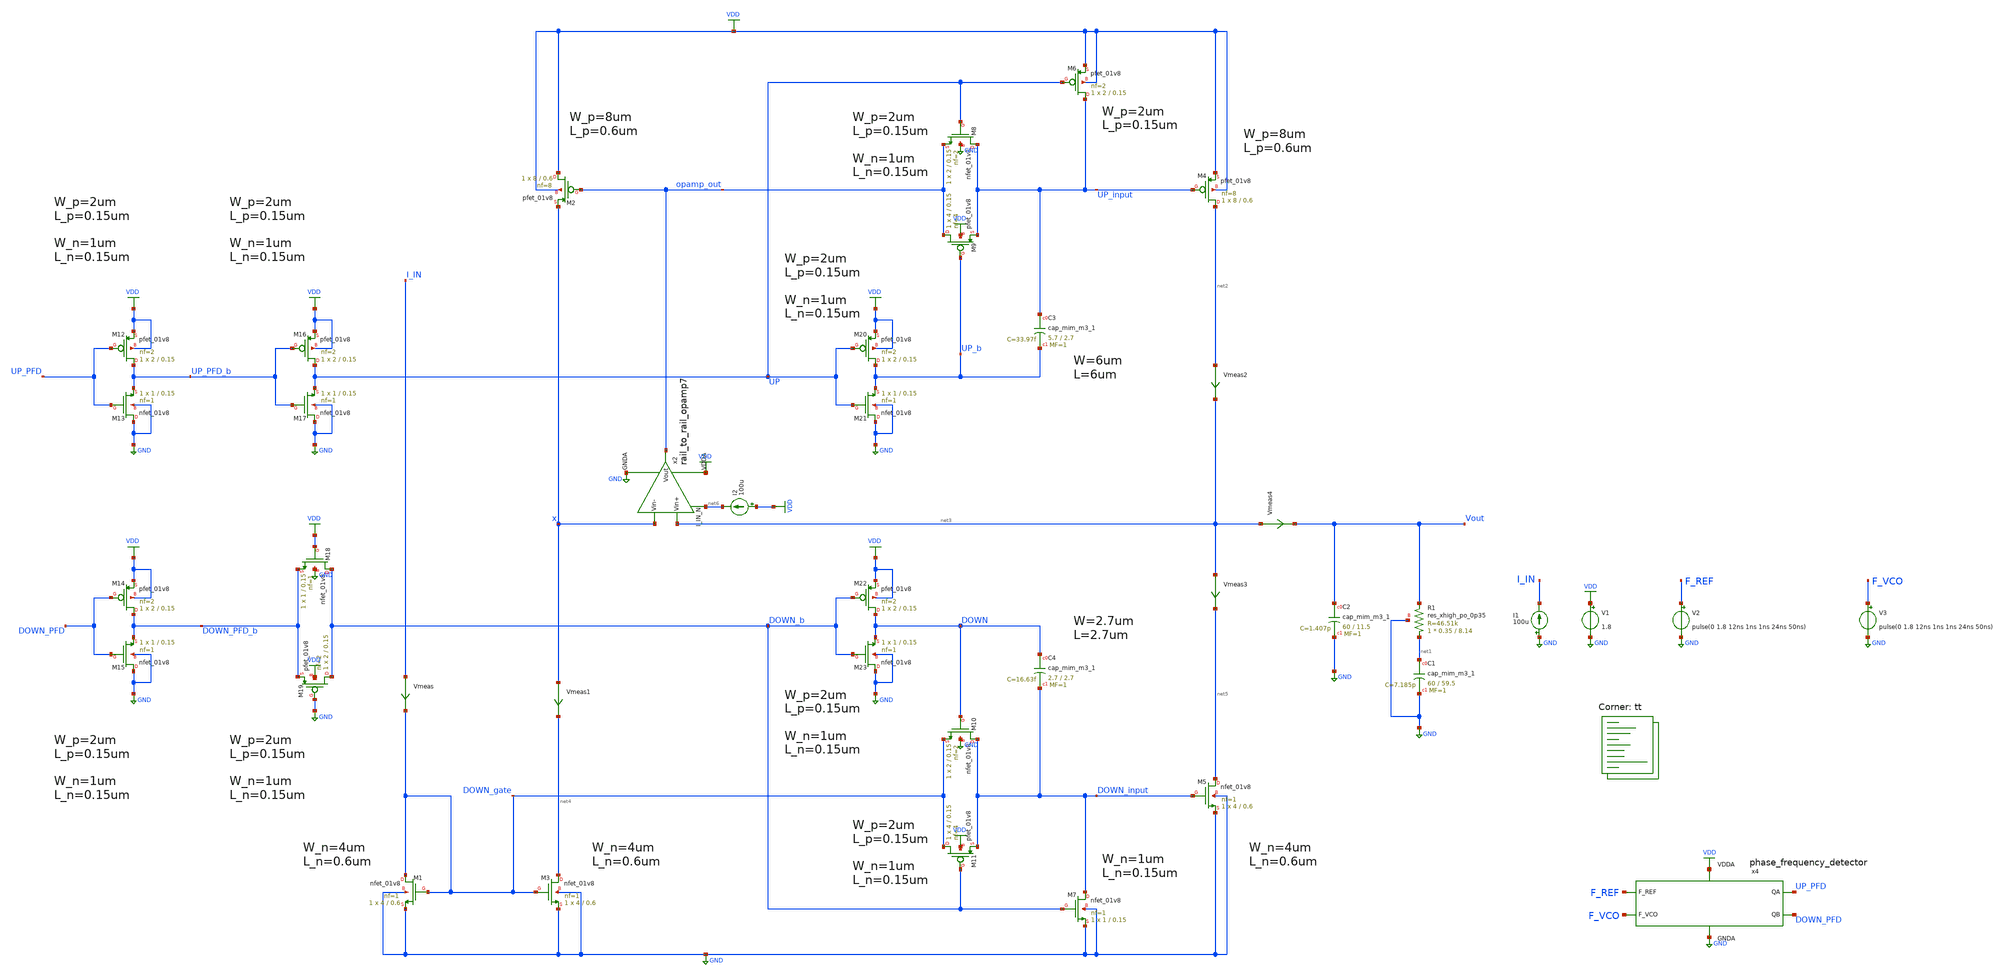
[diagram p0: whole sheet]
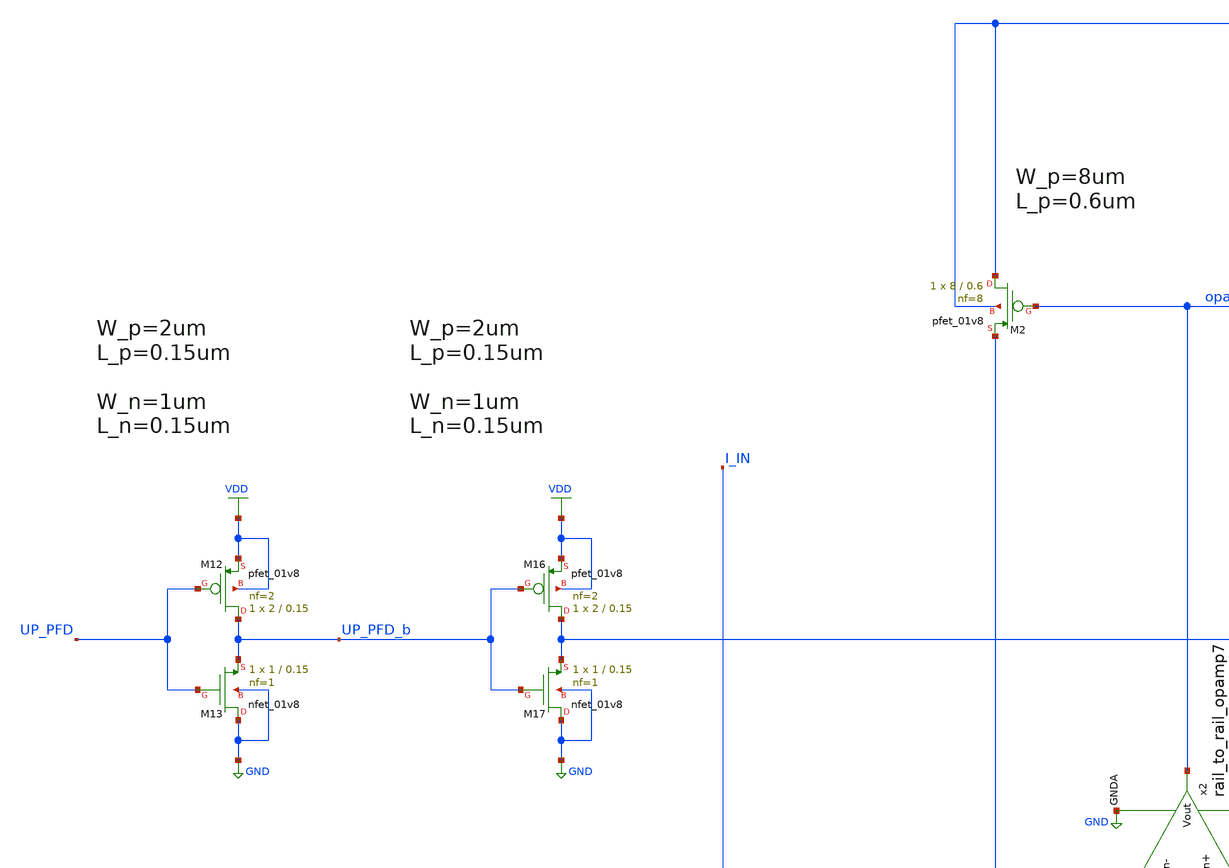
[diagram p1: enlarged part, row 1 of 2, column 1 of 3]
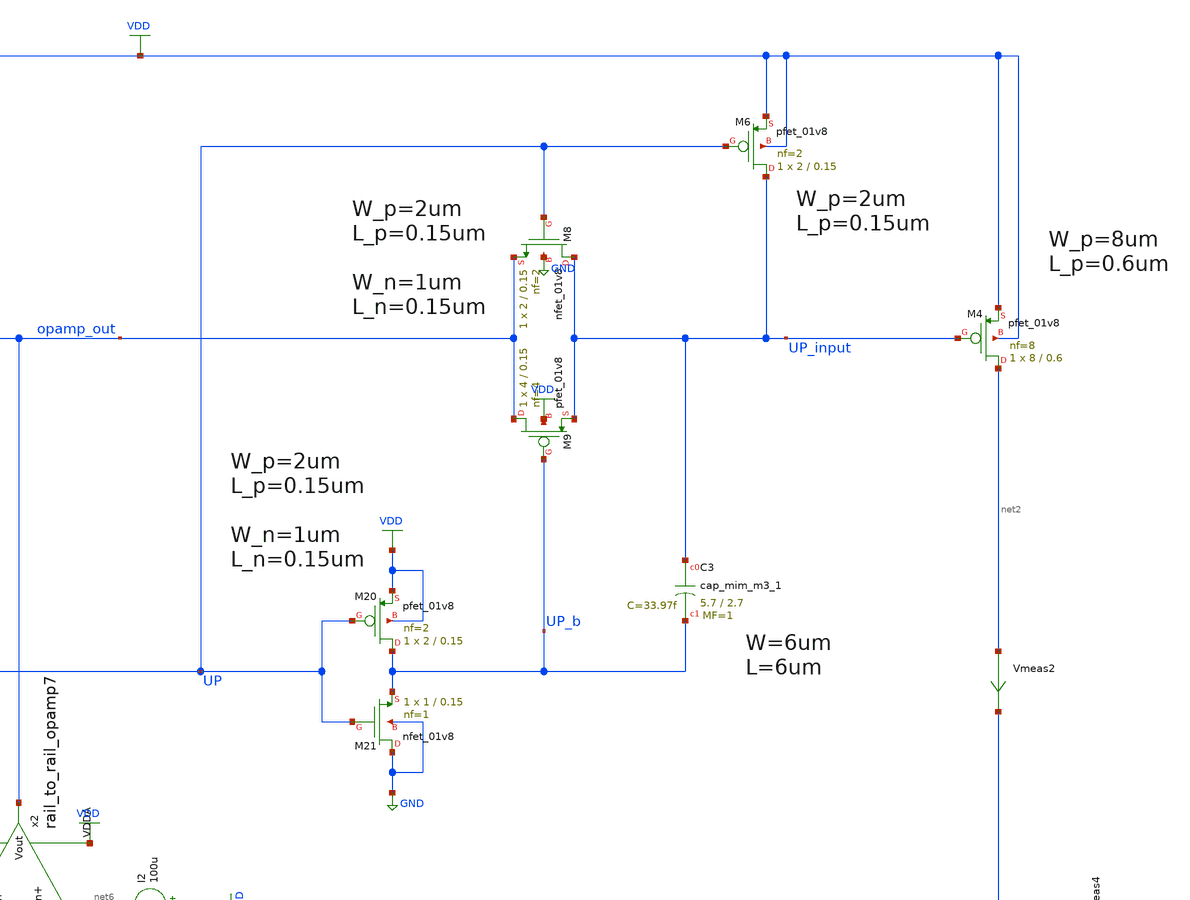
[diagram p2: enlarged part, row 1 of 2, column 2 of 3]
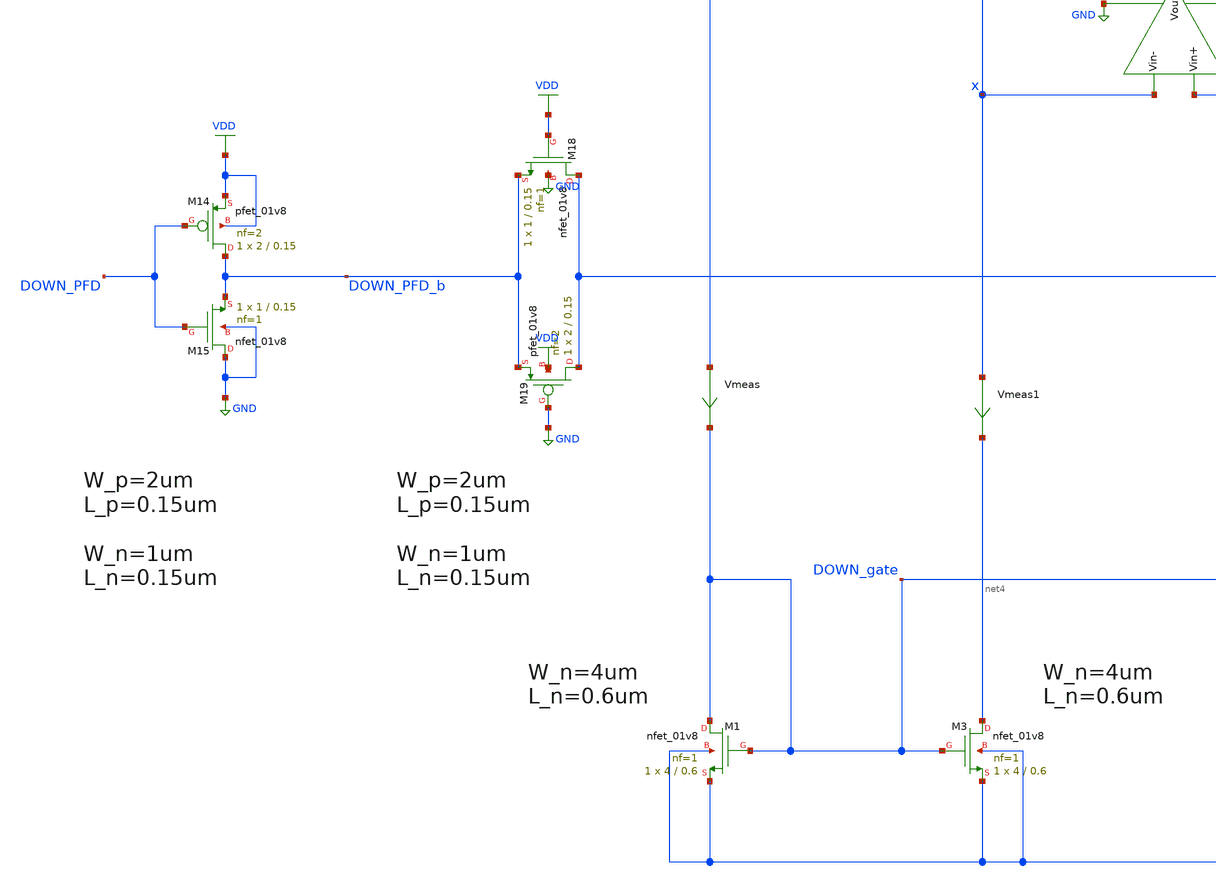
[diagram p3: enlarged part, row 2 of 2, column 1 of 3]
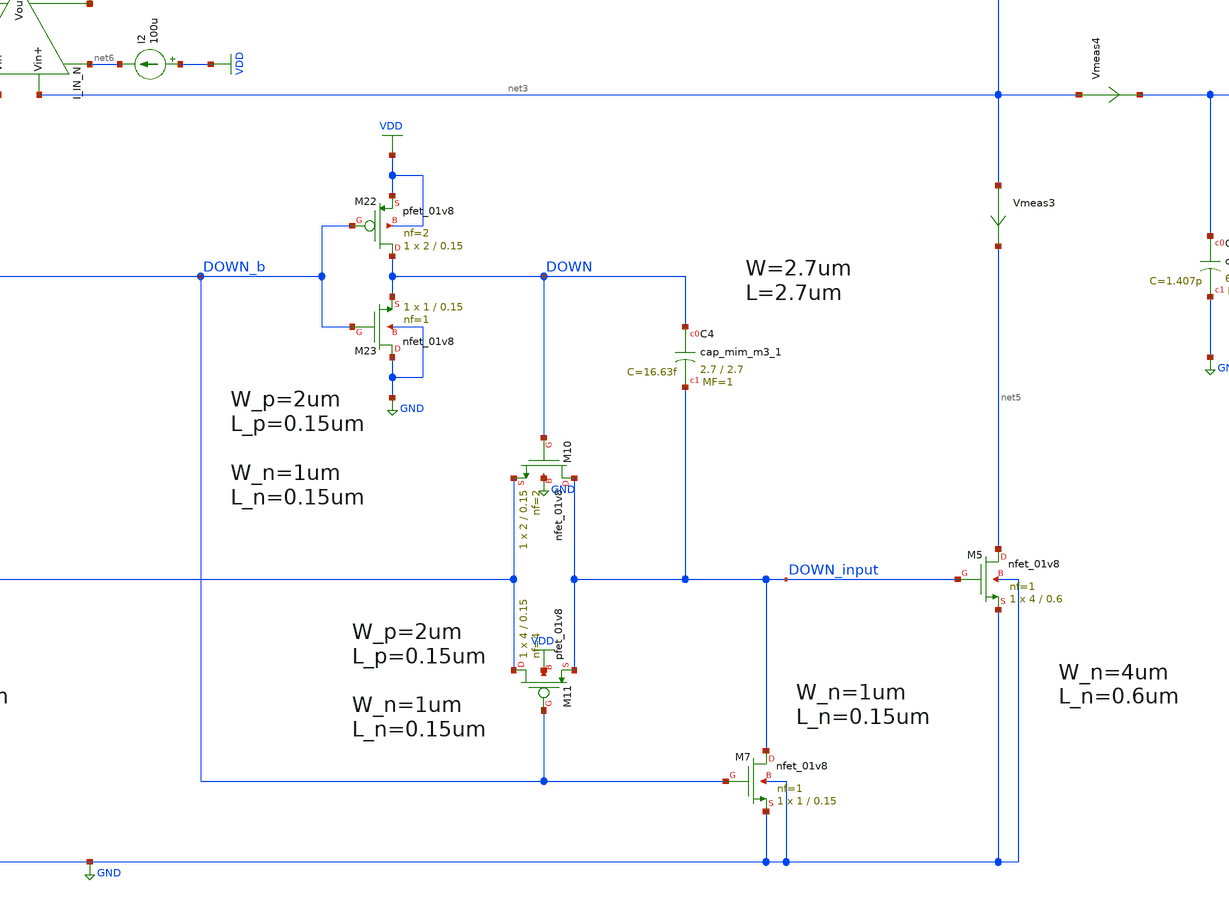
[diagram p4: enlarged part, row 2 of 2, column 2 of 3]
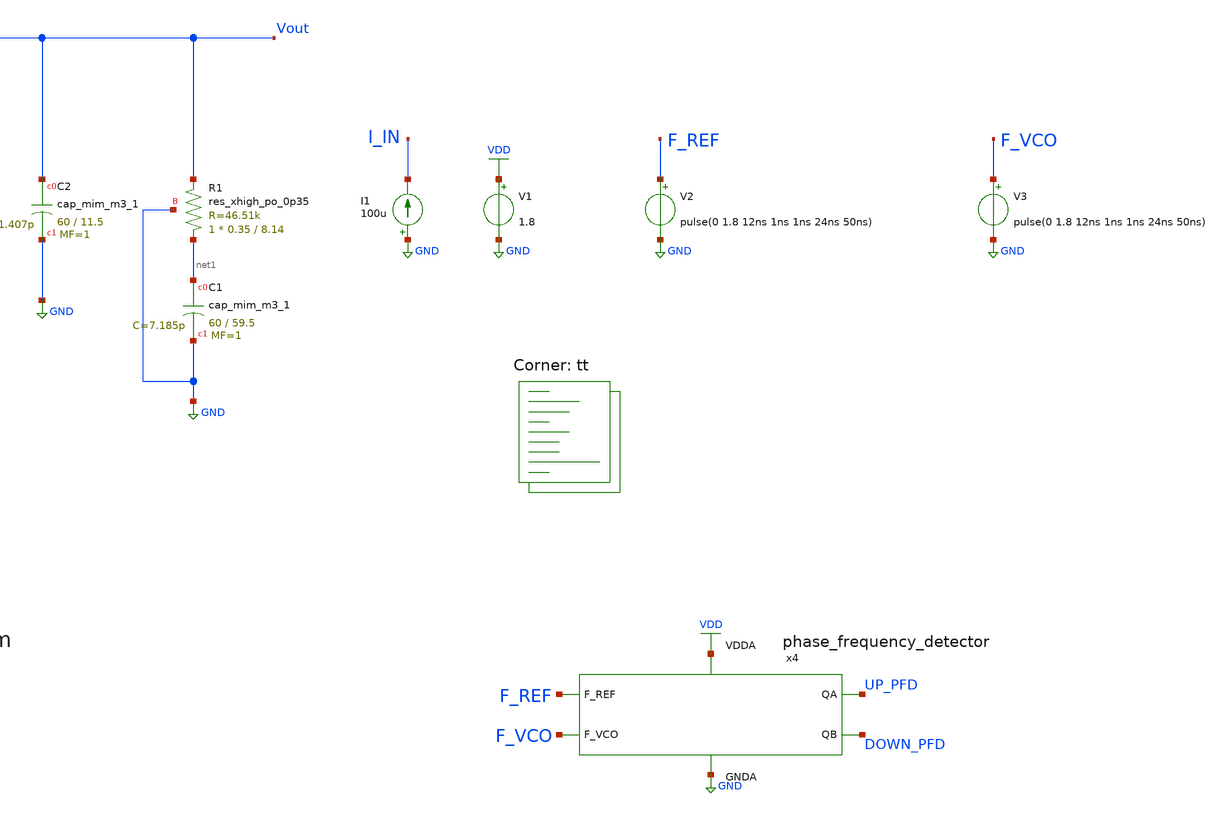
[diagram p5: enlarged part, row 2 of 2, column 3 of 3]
** sch_path: projects/pll/charge_pump/xschem_ngspice/pfd_charge_pump_13.sch
**.subckt pfd_charge_pump_13
V1 VDD GND 1.8
XC2 Vout GND sky130_fd_pr__cap_mim_m3_1 W=60 L=11.5 MF=1 m=1
XC1 net1 GND sky130_fd_pr__cap_mim_m3_1 W=60 L=59.5 MF=1 m=1
V2 F_REF GND pulse(0 1.8 12ns 1ns 1ns 24ns 50ns)
V3 F_VCO GND pulse(0 1.8 12ns 1ns 1ns 24ns 50ns)
x4 F_REF F_VCO VDD UP_PFD DOWN_PFD GND phase_frequency_detector
XR1 net1 Vout GND sky130_fd_pr__res_xhigh_po_0p35 L=8.14 mult=1 m=1
I1 GND I_IN 100u
Vmeas3 net3 net5 0
.save i(vmeas3)
XM1 DOWN_gate DOWN_gate GND GND sky130_fd_pr__nfet_01v8 L=0.6 W=4 nf=1 ad='int((nf+1)/2) * W/nf * 0.29'
+ as='int((nf+2)/2) * W/nf * 0.29' pd='2*int((nf+1)/2) * (W/nf + 0.29)' ps='2*int((nf+2)/2) * (W/nf + 0.29)'
+ nrd='0.29 / W' nrs='0.29 / W' sa=0 sb=0 sd=0 mult=1 m=1
XM3 net4 DOWN_gate GND GND sky130_fd_pr__nfet_01v8 L=0.6 W=4 nf=1 ad='int((nf+1)/2) * W/nf * 0.29' as='int((nf+2)/2) * W/nf * 0.29'
+ pd='2*int((nf+1)/2) * (W/nf + 0.29)' ps='2*int((nf+2)/2) * (W/nf + 0.29)' nrd='0.29 / W' nrs='0.29 / W'
+ sa=0 sb=0 sd=0 mult=1 m=1
XM2 VDD opamp_out x VDD sky130_fd_pr__pfet_01v8 L=0.6 W=8 nf=8 ad='int((nf+1)/2) * W/nf * 0.29' as='int((nf+2)/2) * W/nf * 0.29'
+ pd='2*int((nf+1)/2) * (W/nf + 0.29)' ps='2*int((nf+2)/2) * (W/nf + 0.29)' nrd='0.29 / W' nrs='0.29 / W'
+ sa=0 sb=0 sd=0 mult=1 m=1
XM9 opamp_out UP_b UP_input VDD sky130_fd_pr__pfet_01v8 L=0.15 W=4 nf=4 ad='int((nf+1)/2) * W/nf * 0.29'
+ as='int((nf+2)/2) * W/nf * 0.29' pd='2*int((nf+1)/2) * (W/nf + 0.29)' ps='2*int((nf+2)/2) * (W/nf + 0.29)'
+ nrd='0.29 / W' nrs='0.29 / W' sa=0 sb=0 sd=0 mult=1 m=1
XM6 UP_input UP VDD VDD sky130_fd_pr__pfet_01v8 L=0.15 W=2 nf=2 ad='int((nf+1)/2) * W/nf * 0.29' as='int((nf+2)/2) * W/nf * 0.29'
+ pd='2*int((nf+1)/2) * (W/nf + 0.29)' ps='2*int((nf+2)/2) * (W/nf + 0.29)' nrd='0.29 / W' nrs='0.29 / W'
+ sa=0 sb=0 sd=0 mult=1 m=1
XM4 net2 UP_input VDD VDD sky130_fd_pr__pfet_01v8 L=0.6 W=8 nf=8 ad='int((nf+1)/2) * W/nf * 0.29' as='int((nf+2)/2) * W/nf * 0.29'
+ pd='2*int((nf+1)/2) * (W/nf + 0.29)' ps='2*int((nf+2)/2) * (W/nf + 0.29)' nrd='0.29 / W' nrs='0.29 / W'
+ sa=0 sb=0 sd=0 mult=1 m=1
XM10 DOWN_input DOWN DOWN_gate GND sky130_fd_pr__nfet_01v8 L=0.15 W=2 nf=2 ad='int((nf+1)/2) * W/nf * 0.29'
+ as='int((nf+2)/2) * W/nf * 0.29' pd='2*int((nf+1)/2) * (W/nf + 0.29)' ps='2*int((nf+2)/2) * (W/nf + 0.29)'
+ nrd='0.29 / W' nrs='0.29 / W' sa=0 sb=0 sd=0 mult=1 m=1
XM7 DOWN_input DOWN_b GND GND sky130_fd_pr__nfet_01v8 L=0.15 W=1 nf=1 ad='int((nf+1)/2) * W/nf * 0.29'
+ as='int((nf+2)/2) * W/nf * 0.29' pd='2*int((nf+1)/2) * (W/nf + 0.29)' ps='2*int((nf+2)/2) * (W/nf + 0.29)'
+ nrd='0.29 / W' nrs='0.29 / W' sa=0 sb=0 sd=0 mult=1 m=1
XM5 net5 DOWN_input GND GND sky130_fd_pr__nfet_01v8 L=0.6 W=4 nf=1 ad='int((nf+1)/2) * W/nf * 0.29' as='int((nf+2)/2) * W/nf * 0.29'
+ pd='2*int((nf+1)/2) * (W/nf + 0.29)' ps='2*int((nf+2)/2) * (W/nf + 0.29)' nrd='0.29 / W' nrs='0.29 / W'
+ sa=0 sb=0 sd=0 mult=1 m=1
x2 net6 VDD net3 x opamp_out GND rail_to_rail_opamp7
XM19 DOWN_b GND DOWN_PFD_b VDD sky130_fd_pr__pfet_01v8 L=0.15 W=2 nf=2 ad='int((nf+1)/2) * W/nf * 0.29'
+ as='int((nf+2)/2) * W/nf * 0.29' pd='2*int((nf+1)/2) * (W/nf + 0.29)' ps='2*int((nf+2)/2) * (W/nf + 0.29)'
+ nrd='0.29 / W' nrs='0.29 / W' sa=0 sb=0 sd=0 mult=1 m=1
XM18 DOWN_b VDD DOWN_PFD_b GND sky130_fd_pr__nfet_01v8 L=0.15 W=1 nf=1 ad='int((nf+1)/2) * W/nf * 0.29'
+ as='int((nf+2)/2) * W/nf * 0.29' pd='2*int((nf+1)/2) * (W/nf + 0.29)' ps='2*int((nf+2)/2) * (W/nf + 0.29)'
+ nrd='0.29 / W' nrs='0.29 / W' sa=0 sb=0 sd=0 mult=1 m=1
XM14 DOWN_PFD_b DOWN_PFD VDD VDD sky130_fd_pr__pfet_01v8 L=0.15 W=2 nf=2 ad='int((nf+1)/2) * W/nf * 0.29'
+ as='int((nf+2)/2) * W/nf * 0.29' pd='2*int((nf+1)/2) * (W/nf + 0.29)' ps='2*int((nf+2)/2) * (W/nf + 0.29)'
+ nrd='0.29 / W' nrs='0.29 / W' sa=0 sb=0 sd=0 mult=1 m=1
XM15 GND DOWN_PFD DOWN_PFD_b GND sky130_fd_pr__nfet_01v8 L=0.15 W=1 nf=1 ad='int((nf+1)/2) * W/nf * 0.29'
+ as='int((nf+2)/2) * W/nf * 0.29' pd='2*int((nf+1)/2) * (W/nf + 0.29)' ps='2*int((nf+2)/2) * (W/nf + 0.29)'
+ nrd='0.29 / W' nrs='0.29 / W' sa=0 sb=0 sd=0 mult=1 m=1
XM12 UP_PFD_b UP_PFD VDD VDD sky130_fd_pr__pfet_01v8 L=0.15 W=2 nf=2 ad='int((nf+1)/2) * W/nf * 0.29'
+ as='int((nf+2)/2) * W/nf * 0.29' pd='2*int((nf+1)/2) * (W/nf + 0.29)' ps='2*int((nf+2)/2) * (W/nf + 0.29)'
+ nrd='0.29 / W' nrs='0.29 / W' sa=0 sb=0 sd=0 mult=1 m=1
XM13 GND UP_PFD UP_PFD_b GND sky130_fd_pr__nfet_01v8 L=0.15 W=1 nf=1 ad='int((nf+1)/2) * W/nf * 0.29'
+ as='int((nf+2)/2) * W/nf * 0.29' pd='2*int((nf+1)/2) * (W/nf + 0.29)' ps='2*int((nf+2)/2) * (W/nf + 0.29)'
+ nrd='0.29 / W' nrs='0.29 / W' sa=0 sb=0 sd=0 mult=1 m=1
XM16 UP UP_PFD_b VDD VDD sky130_fd_pr__pfet_01v8 L=0.15 W=2 nf=2 ad='int((nf+1)/2) * W/nf * 0.29' as='int((nf+2)/2) * W/nf * 0.29'
+ pd='2*int((nf+1)/2) * (W/nf + 0.29)' ps='2*int((nf+2)/2) * (W/nf + 0.29)' nrd='0.29 / W' nrs='0.29 / W'
+ sa=0 sb=0 sd=0 mult=1 m=1
XM17 GND UP_PFD_b UP GND sky130_fd_pr__nfet_01v8 L=0.15 W=1 nf=1 ad='int((nf+1)/2) * W/nf * 0.29' as='int((nf+2)/2) * W/nf * 0.29'
+ pd='2*int((nf+1)/2) * (W/nf + 0.29)' ps='2*int((nf+2)/2) * (W/nf + 0.29)' nrd='0.29 / W' nrs='0.29 / W'
+ sa=0 sb=0 sd=0 mult=1 m=1
XM22 DOWN DOWN_b VDD VDD sky130_fd_pr__pfet_01v8 L=0.15 W=2 nf=2 ad='int((nf+1)/2) * W/nf * 0.29' as='int((nf+2)/2) * W/nf * 0.29'
+ pd='2*int((nf+1)/2) * (W/nf + 0.29)' ps='2*int((nf+2)/2) * (W/nf + 0.29)' nrd='0.29 / W' nrs='0.29 / W'
+ sa=0 sb=0 sd=0 mult=1 m=1
XM23 GND DOWN_b DOWN GND sky130_fd_pr__nfet_01v8 L=0.15 W=1 nf=1 ad='int((nf+1)/2) * W/nf * 0.29' as='int((nf+2)/2) * W/nf * 0.29'
+ pd='2*int((nf+1)/2) * (W/nf + 0.29)' ps='2*int((nf+2)/2) * (W/nf + 0.29)' nrd='0.29 / W' nrs='0.29 / W'
+ sa=0 sb=0 sd=0 mult=1 m=1
XM20 UP_b UP VDD VDD sky130_fd_pr__pfet_01v8 L=0.15 W=2 nf=2 ad='int((nf+1)/2) * W/nf * 0.29' as='int((nf+2)/2) * W/nf * 0.29'
+ pd='2*int((nf+1)/2) * (W/nf + 0.29)' ps='2*int((nf+2)/2) * (W/nf + 0.29)' nrd='0.29 / W' nrs='0.29 / W'
+ sa=0 sb=0 sd=0 mult=1 m=1
XM21 GND UP UP_b GND sky130_fd_pr__nfet_01v8 L=0.15 W=1 nf=1 ad='int((nf+1)/2) * W/nf * 0.29' as='int((nf+2)/2) * W/nf * 0.29'
+ pd='2*int((nf+1)/2) * (W/nf + 0.29)' ps='2*int((nf+2)/2) * (W/nf + 0.29)' nrd='0.29 / W' nrs='0.29 / W'
+ sa=0 sb=0 sd=0 mult=1 m=1
Vmeas I_IN DOWN_gate 0
.save i(vmeas)
Vmeas1 x net4 0
.save i(vmeas1)
Vmeas2 net2 net3 0
.save i(vmeas2)
Vmeas4 net3 Vout 0
.save i(vmeas4)
XM8 UP_input UP opamp_out GND sky130_fd_pr__nfet_01v8 L=0.15 W=2 nf=2 ad='int((nf+1)/2) * W/nf * 0.29'
+ as='int((nf+2)/2) * W/nf * 0.29' pd='2*int((nf+1)/2) * (W/nf + 0.29)' ps='2*int((nf+2)/2) * (W/nf + 0.29)'
+ nrd='0.29 / W' nrs='0.29 / W' sa=0 sb=0 sd=0 mult=1 m=1
XM11 DOWN_gate DOWN_b DOWN_input VDD sky130_fd_pr__pfet_01v8 L=0.15 W=4 nf=4 ad='int((nf+1)/2) * W/nf * 0.29'
+ as='int((nf+2)/2) * W/nf * 0.29' pd='2*int((nf+1)/2) * (W/nf + 0.29)' ps='2*int((nf+2)/2) * (W/nf + 0.29)'
+ nrd='0.29 / W' nrs='0.29 / W' sa=0 sb=0 sd=0 mult=1 m=1
XC3 UP_input UP_b sky130_fd_pr__cap_mim_m3_1 W=5.7 L=2.7 MF=1 m=1
XC4 DOWN DOWN_input sky130_fd_pr__cap_mim_m3_1 W=2.7 L=2.7 MF=1 m=1
I2 VDD net6 100u
**** begin user architecture code
.lib $::SKYWATER_MODELS/sky130.lib.spice tt



.include /foss/pdks/sky130A/libs.ref/sky130_fd_sc_hd/spice/sky130_fd_sc_hd.spice

.option method=gear
.option wnflag=1
.option savecurrents

.save @m.x2.xm11.msky130_fd_pr__pfet_01v8[gm] @m.x2.xm12.msky130_fd_pr__nfet_01v8[gm]

* V_out initial voltage value for the F_VCO delay of 2ns  (leading)
* .ic v(vout) = 1.8

* V_out initial voltage value for the F_VCO delay of 12ns (lock condition)
.ic v(vout) = 0.83

* V_out initial voltage value for the F_VCO delay of 22ns (lagging)
* .ic v(vout) = 0

.control
  * save v(f_ref) save v(f_vco) save v(i_in) save v(up_pfd) v(down_pfd) v(up_pfd_b) v(down_pfd_b)
+ v(up) v(up_b) v(down) v(down_b) v(x) v(opamp_out) v(up_input) v(down_input) v(down_gate) v(vout)
  save all

  * timestep for exact simulation results
  * tran 5ps 0.5us

  * timestep for faster simulation results
  tran 50ps 0.5us

  remzerovec
  * write pfd_charge_pump_13.raw
  write pfd_charge_pump_13_2.raw
  set appendwrite

.endc



**** end user architecture code
**.ends
.GLOBAL GND
.GLOBAL VDD
.end
